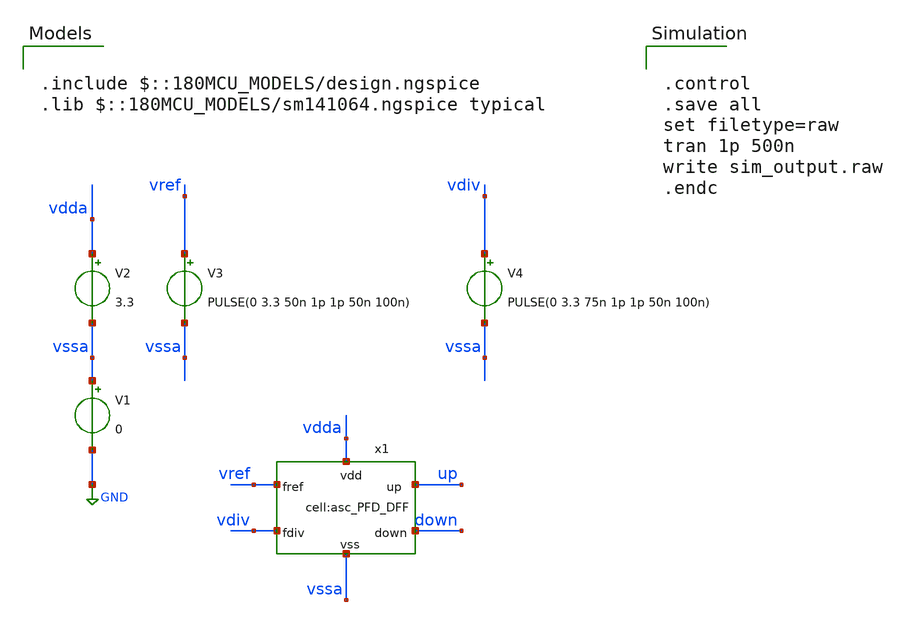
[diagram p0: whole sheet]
** sch_path: designs/libs/tb_analog/tb_asc_PFD_DFF/tb_asc_PFD_DFF.sch
**.subckt tb_asc_PFD_DFF
V1 vssa GND 0
V2 vdda vssa 3.3
V3 vref vssa PULSE(0 3.3 50n 1p 1p 50n 100n)
V4 vdiv vssa PULSE(0 3.3 75n 1p 1p 50n 100n)
x1 vdda vssa down up vref vdiv asc_PFD_DFF
**** begin user architecture code

.include $::180MCU_MODELS/design.ngspice
.lib $::180MCU_MODELS/sm141064.ngspice typical



.control
.save all
set filetype=raw
tran 1p 500n
write sim_output.raw
.endc


**** end user architecture code
**.ends
.GLOBAL GND
.end
